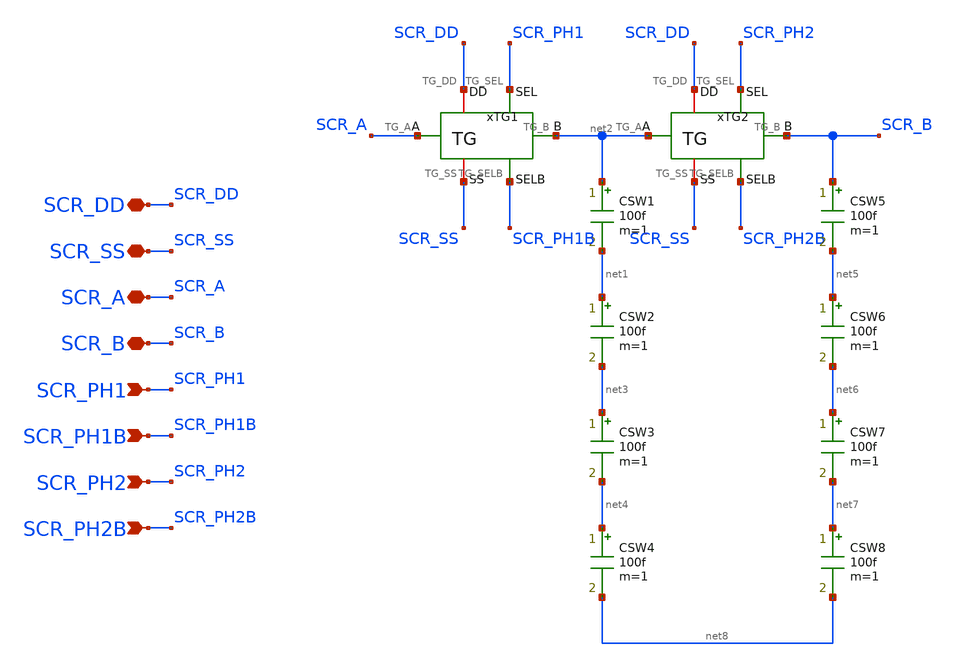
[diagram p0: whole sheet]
** sch_path: Design_Files/IC Design/Schematic/SCR/SCR.sch
**.subckt SCR SCR_DD SCR_SS SCR_PH1 SCR_A SCR_B SCR_PH1B SCR_PH2 SCR_PH2B
*.iopin SCR_DD
*.iopin SCR_SS
*.ipin SCR_PH1
*.iopin SCR_A
*.iopin SCR_B
*.ipin SCR_PH1B
*.ipin SCR_PH2
*.ipin SCR_PH2B
CSW1 net2 net1 100f m=1
xTG1 SCR_DD SCR_SS SCR_A net2 SCR_PH1 SCR_PH1B TG
xTG2 SCR_DD SCR_SS net2 SCR_B SCR_PH2 SCR_PH2B TG
CSW2 net1 net3 100f m=1
CSW3 net3 net4 100f m=1
CSW4 net4 net8 100f m=1
CSW5 SCR_B net5 100f m=1
CSW6 net5 net6 100f m=1
CSW7 net6 net7 100f m=1
CSW8 net7 net8 100f m=1
**.ends

* expanding   symbol:  ECG_Acquisition_IC/Design_Files/IC Design/Schematic/TG/TG.sym # of pins=6
** sym_path: Design_Files/IC Design/Schematic/TG/TG.sym
** sch_path: Design_Files/IC Design/Schematic/TG/TG.sch
.subckt TG TG_DD TG_SS TG_A TG_B TG_SEL TG_SELB
*.iopin TG_DD
*.iopin TG_SS
*.iopin TG_A
*.iopin TG_B
*.ipin TG_SEL
*.ipin TG_SELB
XMTGP TG_B TG_SELB TG_A TG_DD pfet_03v3 L=0.5u W=40u nf=1 ad='int((nf+1)/2) * W/nf * 0.18u' as='int((nf+2)/2) * W/nf * 0.18u'
+ pd='2*int((nf+1)/2) * (W/nf + 0.18u)' ps='2*int((nf+2)/2) * (W/nf + 0.18u)' nrd='0.18u / W' nrs='0.18u / W'
+ sa=0 sb=0 sd=0 m=1
XMTGN TG_A TG_SEL TG_B TG_SS nfet_03v3 L=0.5u W=20u nf=1 ad='int((nf+1)/2) * W/nf * 0.18u' as='int((nf+2)/2) * W/nf * 0.18u'
+ pd='2*int((nf+1)/2) * (W/nf + 0.18u)' ps='2*int((nf+2)/2) * (W/nf + 0.18u)' nrd='0.18u / W' nrs='0.18u / W'
+ sa=0 sb=0 sd=0 m=1
.ends

.end
